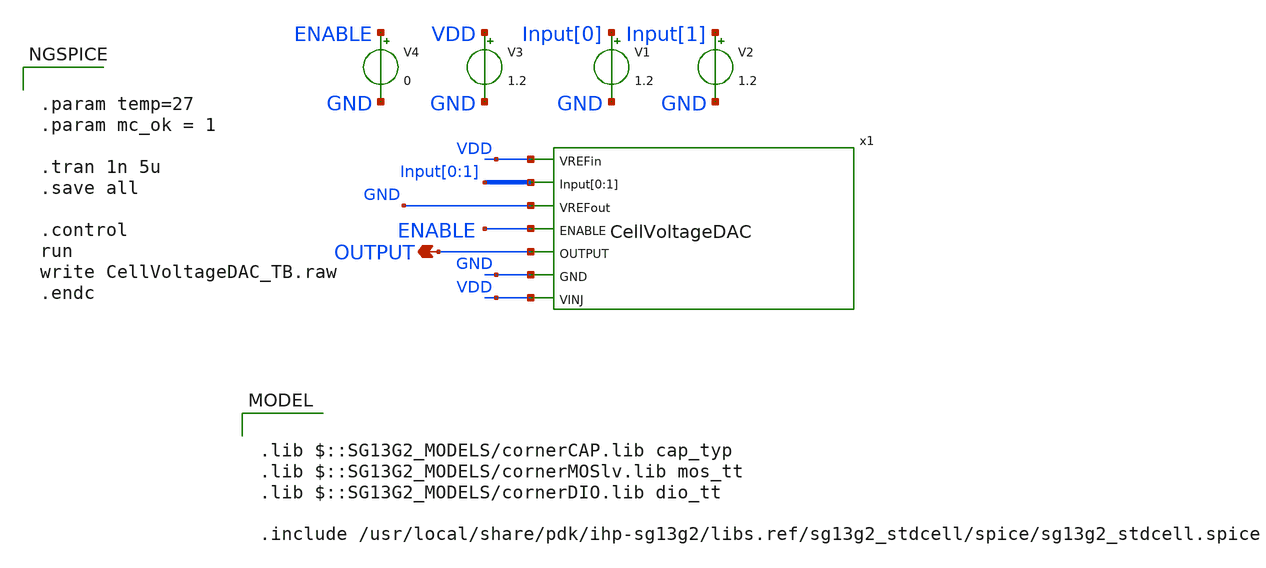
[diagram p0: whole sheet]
** sch_path: ihp130_cells/CellVoltageDAC/CellVoltageDAC_TB.sch
**.subckt CellVoltageDAC_TB OUTPUT
*.opin OUTPUT
x1 VDD Input[0] Input[1] GND ENABLE OUTPUT GND VDD CellVoltageDAC
V3 VDD GND 1.2
V1 Input[0] GND 1.2
V2 Input[1] GND 1.2
V4 ENABLE GND 0
**** begin user architecture code

.lib $::SG13G2_MODELS/cornerCAP.lib cap_typ
.lib $::SG13G2_MODELS/cornerMOSlv.lib mos_tt
.lib $::SG13G2_MODELS/cornerDIO.lib dio_tt

.include /usr/local/share/pdk/ihp-sg13g2/libs.ref/sg13g2_stdcell/spice/sg13g2_stdcell.spice



.param temp=27
.param mc_ok = 1

.tran 1n 5u
.save all

.control
run
write CellVoltageDAC_TB.raw
.endc


**** end user architecture code
**.ends

* expanding   symbol:  CellVoltageDAC/CellVoltageDAC.sym # of pins=7
** sym_path: ihp130_cells/CellVoltageDAC/CellVoltageDAC.sym
** sch_path: ihp130_cells/CellVoltageDAC/CellVoltageDAC.sch
.subckt CellVoltageDAC VREFin Input[0] Input[1] VREFout ENABLE OUTPUT GND VINJ
*.ipin Input[0],Input[1]
*.ipin ENABLE
*.ipin GND
*.ipin VINJ
*.ipin VREFin
*.ipin VREFout
*.ipin OUTPUT
x1 VREFout VREFin OUTPUT GND VINJ net1[3] net1[2] net1[1] net1[0] ihp130_DAC_cell
x2 Input[0] Input[1] ENABLE net1[3] net1[2] net1[1] net1[0] GND VINJ ihp130_VinjDec2_to_4
.ends


* expanding   symbol:  DAC_Cell/ihp130_DAC_cell.sym # of pins=6
** sym_path: ihp130_cells/DAC_Cell/ihp130_DAC_cell.sym
** sch_path: ihp130_cells/DAC_Cell/ihp130_DAC_cell.sch
.subckt ihp130_DAC_cell VREFout VREFin OUTPUT GND VINJ SELECT[0] SELECT[1] SELECT[2] SELECT[3]
*.ipin GND
*.ipin VINJ
*.ipin SELECT[0],SELECT[1],SELECT[2],SELECT[3]
*.ipin VREFin
*.opin VREFout
*.opin OUTPUT
x1 SELECT[0] SELECT[1] SELECT[2] SELECT[3] OUTPUT INPUT[0] INPUT[1] INPUT[2] INPUT[3] VINJ GND
+ 4TgateVinj
x2 VREFin INPUT[0] INPUT[1] INPUT[2] INPUT[3] VREFout ihp130_resistor_string
.ends


* expanding   symbol:  VinjDec2_to_4/ihp130_VinjDec2_to_4.sym # of pins=5
** sym_path: ihp130_cells/VinjDec2_to_4/ihp130_VinjDec2_to_4.sym
** sch_path: ihp130_cells/VinjDec2_to_4/ihp130_VinjDec2_to_4.sch
.subckt ihp130_VinjDec2_to_4 Input[0] Input[1] ENABLE Output[0] Output[1] Output[2] Output[3] GND
+ VINJ
*.ipin VINJ
*.opin Output[0],Output[1],Output[2],Output[3]
*.ipin Input[0],Input[1]
*.ipin GND
*.ipin ENABLE
x2 VINJ Input[0] net1 GND ihp130_VinjInv2
x6 VINJ Input[1] net2 GND ihp130_VinjInv2
x7 VINJ ENABLE ENABLE_B GND ihp130_VinjInv2
x1 VINJ Input[0] Input[1] Output[0] ENABLE_B GND ihp130_VinjNOR3
x3 VINJ Input[0] net2 Output[1] ENABLE_B GND ihp130_VinjNOR3
x4 VINJ net1 Input[1] Output[2] ENABLE_B GND ihp130_VinjNOR3
x5 VINJ net1 net2 Output[3] ENABLE_B GND ihp130_VinjNOR3
.ends


* expanding   symbol:  4TgateVinj/4TgateVinj.sym # of pins=5
** sym_path: ihp130_cells/4TgateVinj/4TgateVinj.sym
** sch_path: ihp130_cells/4TgateVinj/4TgateVinj.sch
.subckt 4TgateVinj SELECT[0] SELECT[1] SELECT[2] SELECT[3] OUTPUT INPUT[0] INPUT[1] INPUT[2]
+ INPUT[3] VINJ GND
*.ipin SELECT[0],SELECT[1],SELECT[2],SELECT[3]
*.ipin INPUT[0],INPUT[1],INPUT[2],INPUT[3]
*.ipin VINJ
*.ipin GND
*.opin OUTPUT
x1 SELECT[0] INPUT[0] VINJ GND OUTPUT ihp130_TgateVinj02
x2 SELECT[1] INPUT[1] VINJ GND OUTPUT ihp130_TgateVinj02
x3 SELECT[2] INPUT[2] VINJ GND OUTPUT ihp130_TgateVinj02
x4 SELECT[3] INPUT[3] VINJ GND OUTPUT ihp130_TgateVinj02
.ends


* expanding   symbol:  Resistor_String/ihp130_resistor_string.sym # of pins=3
** sym_path: ihp130_cells/Resistor_String/ihp130_resistor_string.sym
** sch_path: ihp130_cells/Resistor_String/ihp130_resistor_string.sch
.subckt ihp130_resistor_string VREFin Node[0] Node[1] Node[2] Node[3] VREFout
*.iopin VREFout
*.iopin VREFin
*.opin Node[0],Node[1],Node[2],Node[3]
XR8 VREFin Node[0] sub! rsil w=.59e-6 l=10e-6 m=1 mm_ok=1
XR1 Node[0] net1 sub! rsil w=.59e-6 l=10e-6 m=1 mm_ok=1
XR2 net1 Node[1] sub! rsil w=.59e-6 l=10e-6 m=1 mm_ok=1
XR3 Node[1] net2 sub! rsil w=.59e-6 l=10e-6 m=1 mm_ok=1
XR4 net2 Node[2] sub! rsil w=.59e-6 l=10e-6 m=1 mm_ok=1
XR5 Node[2] net3 sub! rsil w=.59e-6 l=10e-6 m=1 mm_ok=1
XR6 net3 Node[3] sub! rsil w=.59e-6 l=10e-6 m=1 mm_ok=1
XR7 Node[3] VREFout sub! rsil w=.59e-6 l=10e-6 m=1 mm_ok=1
.ends


* expanding   symbol:  VinjInv2/ihp130_VinjInv2.sym # of pins=4
** sym_path: ihp130_cells/VinjInv2/ihp130_VinjInv2.sym
** sch_path: ihp130_cells/VinjInv2/ihp130_VinjInv2.sch
.subckt ihp130_VinjInv2 VINJ Input Output GND
*.ipin VINJ
*.ipin GND
*.ipin Input
*.opin Output
XM1 Output Input GND GND sg13_hv_nmos w=0.42u l=0.53u ng=1 m=1 mm_ok=1
XM2 Output Input VINJ VINJ sg13_hv_pmos w=0.42u l=0.53u ng=1 m=1 mm_ok=1
.ends


* expanding   symbol:  VinjNOR3/ihp130_VinjNOR3.sym # of pins=6
** sym_path: ihp130_cells/VinjNOR3/ihp130_VinjNOR3.sym
** sch_path: ihp130_cells/VinjNOR3/ihp130_VinjNOR3.sch
.subckt ihp130_VinjNOR3 VINJ Input[0] Input[1] Output Input[2] GND
*.ipin Input[0]
*.ipin VINJ
*.ipin GND
*.opin Output
*.ipin Input[1]
*.ipin Input[2]
XM1 net1 Input[2] VINJ VINJ sg13_hv_pmos w=0.42u l=0.53u ng=1 m=1 mm_ok=1
XM2 net2 Input[0] net1 VINJ sg13_hv_pmos w=0.42u l=0.53u ng=1 m=1 mm_ok=1
XM3 Output Input[1] net2 VINJ sg13_hv_pmos w=0.42u l=0.53u ng=1 m=1 mm_ok=1
XM4 Output Input[1] GND GND sg13_hv_nmos w=0.42u l=0.5u ng=1 m=1 mm_ok=1
XM5 Output Input[2] GND GND sg13_hv_nmos w=0.42u l=0.5u ng=1 m=1 mm_ok=1
XM6 Output Input[0] GND GND sg13_hv_nmos w=0.42u l=0.5u ng=1 m=1 mm_ok=1
.ends


* expanding   symbol:  TgateVinj02/ihp130_TgateVinj02.sym # of pins=5
** sym_path: ihp130_cells/TgateVinj02/ihp130_TgateVinj02.sym
** sch_path: ihp130_cells/TgateVinj02/ihp130_TgateVinj02.sch
.subckt ihp130_TgateVinj02 SELECT INPUT VINJ GND OUTPUT
*.ipin SELECT
*.ipin INPUT
*.ipin VINJ
*.ipin GND
*.opin OUTPUT
XM1 Selb SELECT VINJ VINJ sg13_hv_pmos w=0.42u l=0.5u ng=1 m=1 mm_ok=1
XM2 Selb SELECT GND GND sg13_hv_nmos w=0.42u l=0.5u ng=1 m=1 mm_ok=1
XM3 INPUT Selb OUTPUT VINJ sg13_hv_pmos w=0.42u l=0.5u ng=1 m=1 mm_ok=1
XM4 INPUT SELECT OUTPUT GND sg13_hv_nmos w=0.42u l=0.5u ng=1 m=1 mm_ok=1
.ends

.end
